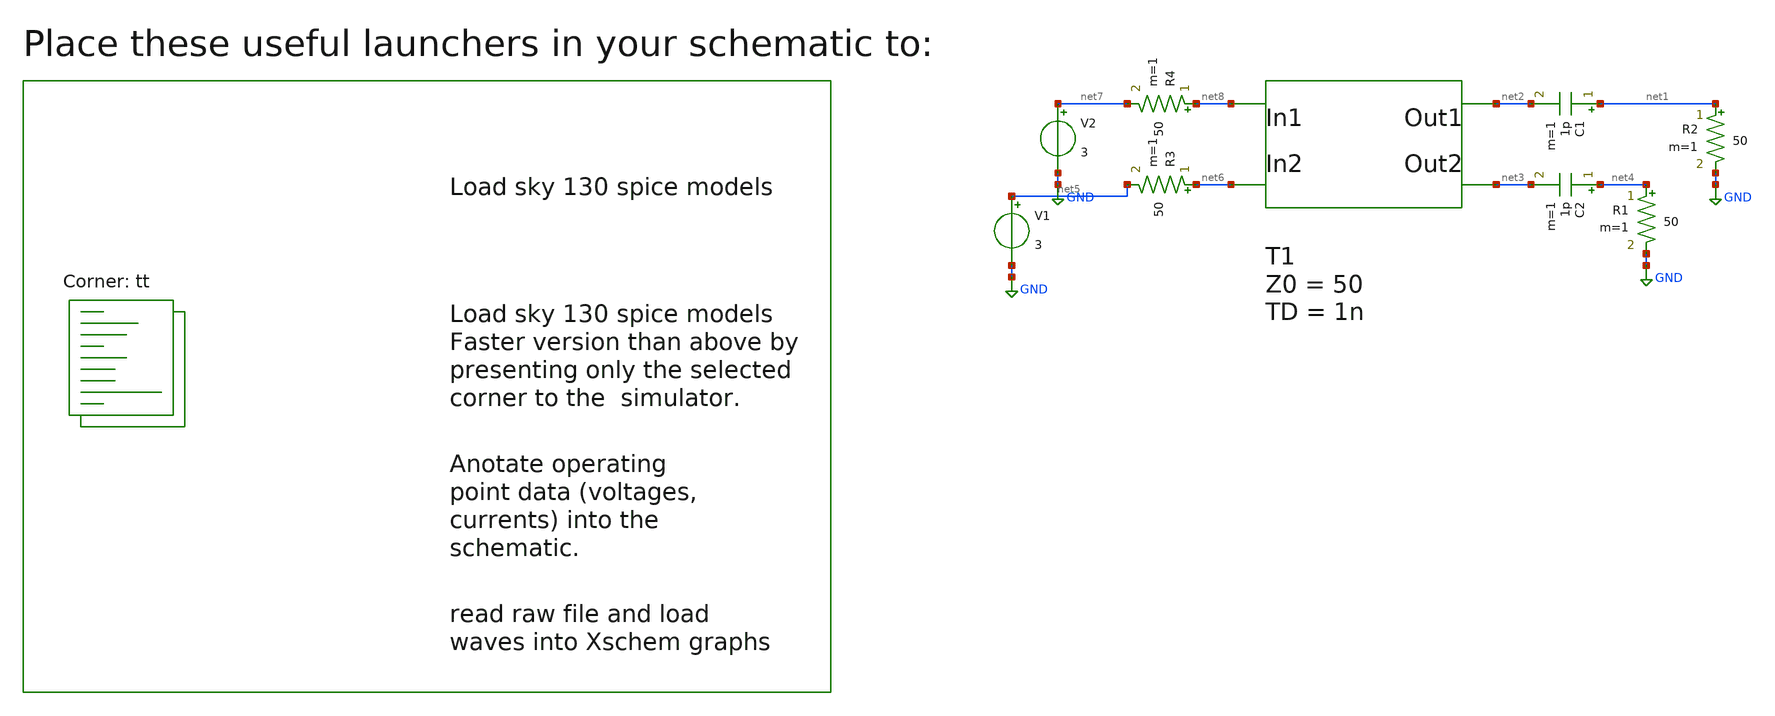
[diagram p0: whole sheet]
** sch_path: termination_resistor/termination.sch
**.subckt termination
T1 net8 net6 net2 net3 Z0=50 TD=1n
R1 net4 GND 50 m=1
R2 net1 GND 50 m=1
C1 net1 net2 1p m=1
C2 net4 net3 1p m=1
R3 net6 net5 50 m=1
R4 net8 net7 50 m=1
V1 net5 GND 3
V2 net7 GND 3
**** begin user architecture code

** opencircuitdesign pdks install
.lib $::SKYWATER_MODELS/sky130.lib.spice tt

.lib $::SKYWATER_MODELS/sky130.lib.spice tt
**** end user architecture code
**.ends
.GLOBAL GND
.end
